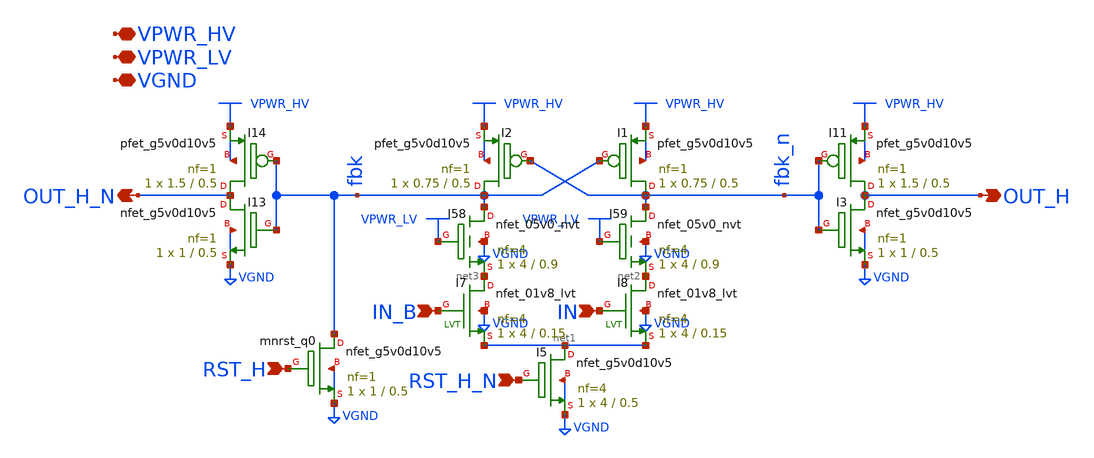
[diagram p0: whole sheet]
** sch_path: gpiov2_amux_ctl_ls.sch
* Copyright 2023 David Mitchell Bailey
* Licensed under the Apache License, Version 2.0 (the "License");
* you may not use this file except in compliance with the License.
* You may obtain a copy of the License at
* https://www.apache.org/licenses/LICENSE-2.0
* Unless required by applicable law or agreed to in writing, software
* distributed under the License is distributed on an "AS IS" BASIS,
* WITHOUT WARRANTIES OR CONDITIONS OF ANY KIND, either express or implied.
* See the License for the specific language governing permissions and
* limitations under the License.
**.subckt gpiov2_amux_ctl_ls RST_H OUT_H VPWR_LV VGND OUT_H_N RST_H_N IN_B IN VPWR_HV
*.ipin RST_H
*.opin OUT_H
*.iopin VPWR_LV
*.iopin VGND
*.opin OUT_H_N
*.ipin RST_H_N
*.ipin IN_B
*.ipin IN
*.iopin VPWR_HV
XI13 OUT_H_N fbk VGND VGND sky130_fd_pr__nfet_g5v0d10v5 L=0.5 W=1 nf=1 ad='int((nf+1)/2) * W/nf * 0.29'
+ as='int((nf+2)/2) * W/nf * 0.29' pd='2*int((nf+1)/2) * (W/nf + 0.29)' ps='2*int((nf+2)/2) * (W/nf + 0.29)'
+ nrd='0.29 / W' nrs='0.29 / W' sa=0 sb=0 sd=0 mult=1 m=1
XI14 OUT_H_N fbk VPWR_HV VPWR_HV sky130_fd_pr__pfet_g5v0d10v5 L=0.5 W=1.5 nf=1 ad='int((nf+1)/2) * W/nf * 0.29'
+ as='int((nf+2)/2) * W/nf * 0.29' pd='2*int((nf+1)/2) * (W/nf + 0.29)' ps='2*int((nf+2)/2) * (W/nf + 0.29)'
+ nrd='0.29 / W' nrs='0.29 / W' sa=0 sb=0 sd=0 mult=1 m=1
XI3 OUT_H fbk_n VGND VGND sky130_fd_pr__nfet_g5v0d10v5 L=0.5 W=1 nf=1 ad='int((nf+1)/2) * W/nf * 0.29'
+ as='int((nf+2)/2) * W/nf * 0.29' pd='2*int((nf+1)/2) * (W/nf + 0.29)' ps='2*int((nf+2)/2) * (W/nf + 0.29)'
+ nrd='0.29 / W' nrs='0.29 / W' sa=0 sb=0 sd=0 mult=1 m=1
XI11 OUT_H fbk_n VPWR_HV VPWR_HV sky130_fd_pr__pfet_g5v0d10v5 L=0.5 W=1.5 nf=1 ad='int((nf+1)/2) * W/nf * 0.29'
+ as='int((nf+2)/2) * W/nf * 0.29' pd='2*int((nf+1)/2) * (W/nf + 0.29)' ps='2*int((nf+2)/2) * (W/nf + 0.29)'
+ nrd='0.29 / W' nrs='0.29 / W' sa=0 sb=0 sd=0 mult=1 m=1
XI1 fbk_n fbk VPWR_HV VPWR_HV sky130_fd_pr__pfet_g5v0d10v5 L=0.5 W=0.75 nf=1 ad='int((nf+1)/2) * W/nf * 0.29'
+ as='int((nf+2)/2) * W/nf * 0.29' pd='2*int((nf+1)/2) * (W/nf + 0.29)' ps='2*int((nf+2)/2) * (W/nf + 0.29)'
+ nrd='0.29 / W' nrs='0.29 / W' sa=0 sb=0 sd=0 mult=1 m=1
XI2 fbk fbk_n VPWR_HV VPWR_HV sky130_fd_pr__pfet_g5v0d10v5 L=0.5 W=0.75 nf=1 ad='int((nf+1)/2) * W/nf * 0.29'
+ as='int((nf+2)/2) * W/nf * 0.29' pd='2*int((nf+1)/2) * (W/nf + 0.29)' ps='2*int((nf+2)/2) * (W/nf + 0.29)'
+ nrd='0.29 / W' nrs='0.29 / W' sa=0 sb=0 sd=0 mult=1 m=1
Xmnrst_q0 fbk RST_H VGND VGND sky130_fd_pr__nfet_g5v0d10v5 L=0.5 W=1 nf=1 ad='int((nf+1)/2) * W/nf * 0.29'
+ as='int((nf+2)/2) * W/nf * 0.29' pd='2*int((nf+1)/2) * (W/nf + 0.29)' ps='2*int((nf+2)/2) * (W/nf + 0.29)'
+ nrd='0.29 / W' nrs='0.29 / W' sa=0 sb=0 sd=0 mult=1 m=1
XI5 net1 RST_H_N VGND VGND sky130_fd_pr__nfet_g5v0d10v5 L=0.5 W=4 nf=4 ad='int((nf+1)/2) * W/nf * 0.29'
+ as='int((nf+2)/2) * W/nf * 0.29' pd='2*int((nf+1)/2) * (W/nf + 0.29)' ps='2*int((nf+2)/2) * (W/nf + 0.29)'
+ nrd='0.29 / W' nrs='0.29 / W' sa=0 sb=0 sd=0 mult=1 m=1
XI59 fbk_n VPWR_LV net2 VGND sky130_fd_pr__nfet_05v0_nvt L=0.9 W=4 nf=4 ad='int((nf+1)/2) * W/nf * 0.29'
+ as='int((nf+2)/2) * W/nf * 0.29' pd='2*int((nf+1)/2) * (W/nf + 0.29)' ps='2*int((nf+2)/2) * (W/nf + 0.29)'
+ nrd='0.29 / W' nrs='0.29 / W' sa=0 sb=0 sd=0 mult=1 m=1
XI58 fbk VPWR_LV net3 VGND sky130_fd_pr__nfet_05v0_nvt L=0.9 W=4 nf=4 ad='int((nf+1)/2) * W/nf * 0.29'
+ as='int((nf+2)/2) * W/nf * 0.29' pd='2*int((nf+1)/2) * (W/nf + 0.29)' ps='2*int((nf+2)/2) * (W/nf + 0.29)'
+ nrd='0.29 / W' nrs='0.29 / W' sa=0 sb=0 sd=0 mult=1 m=1
XI8 net2 IN net1 VGND sky130_fd_pr__nfet_01v8_lvt L=0.15 W=4 nf=4 ad='int((nf+1)/2) * W/nf * 0.29' as='int((nf+2)/2) * W/nf * 0.29'
+ pd='2*int((nf+1)/2) * (W/nf + 0.29)' ps='2*int((nf+2)/2) * (W/nf + 0.29)' nrd='0.29 / W' nrs='0.29 / W'
+ sa=0 sb=0 sd=0 mult=1 m=1
XI7 net3 IN_B net1 VGND sky130_fd_pr__nfet_01v8_lvt L=0.15 W=4 nf=4 ad='int((nf+1)/2) * W/nf * 0.29'
+ as='int((nf+2)/2) * W/nf * 0.29' pd='2*int((nf+1)/2) * (W/nf + 0.29)' ps='2*int((nf+2)/2) * (W/nf + 0.29)'
+ nrd='0.29 / W' nrs='0.29 / W' sa=0 sb=0 sd=0 mult=1 m=1
**.ends
.end
